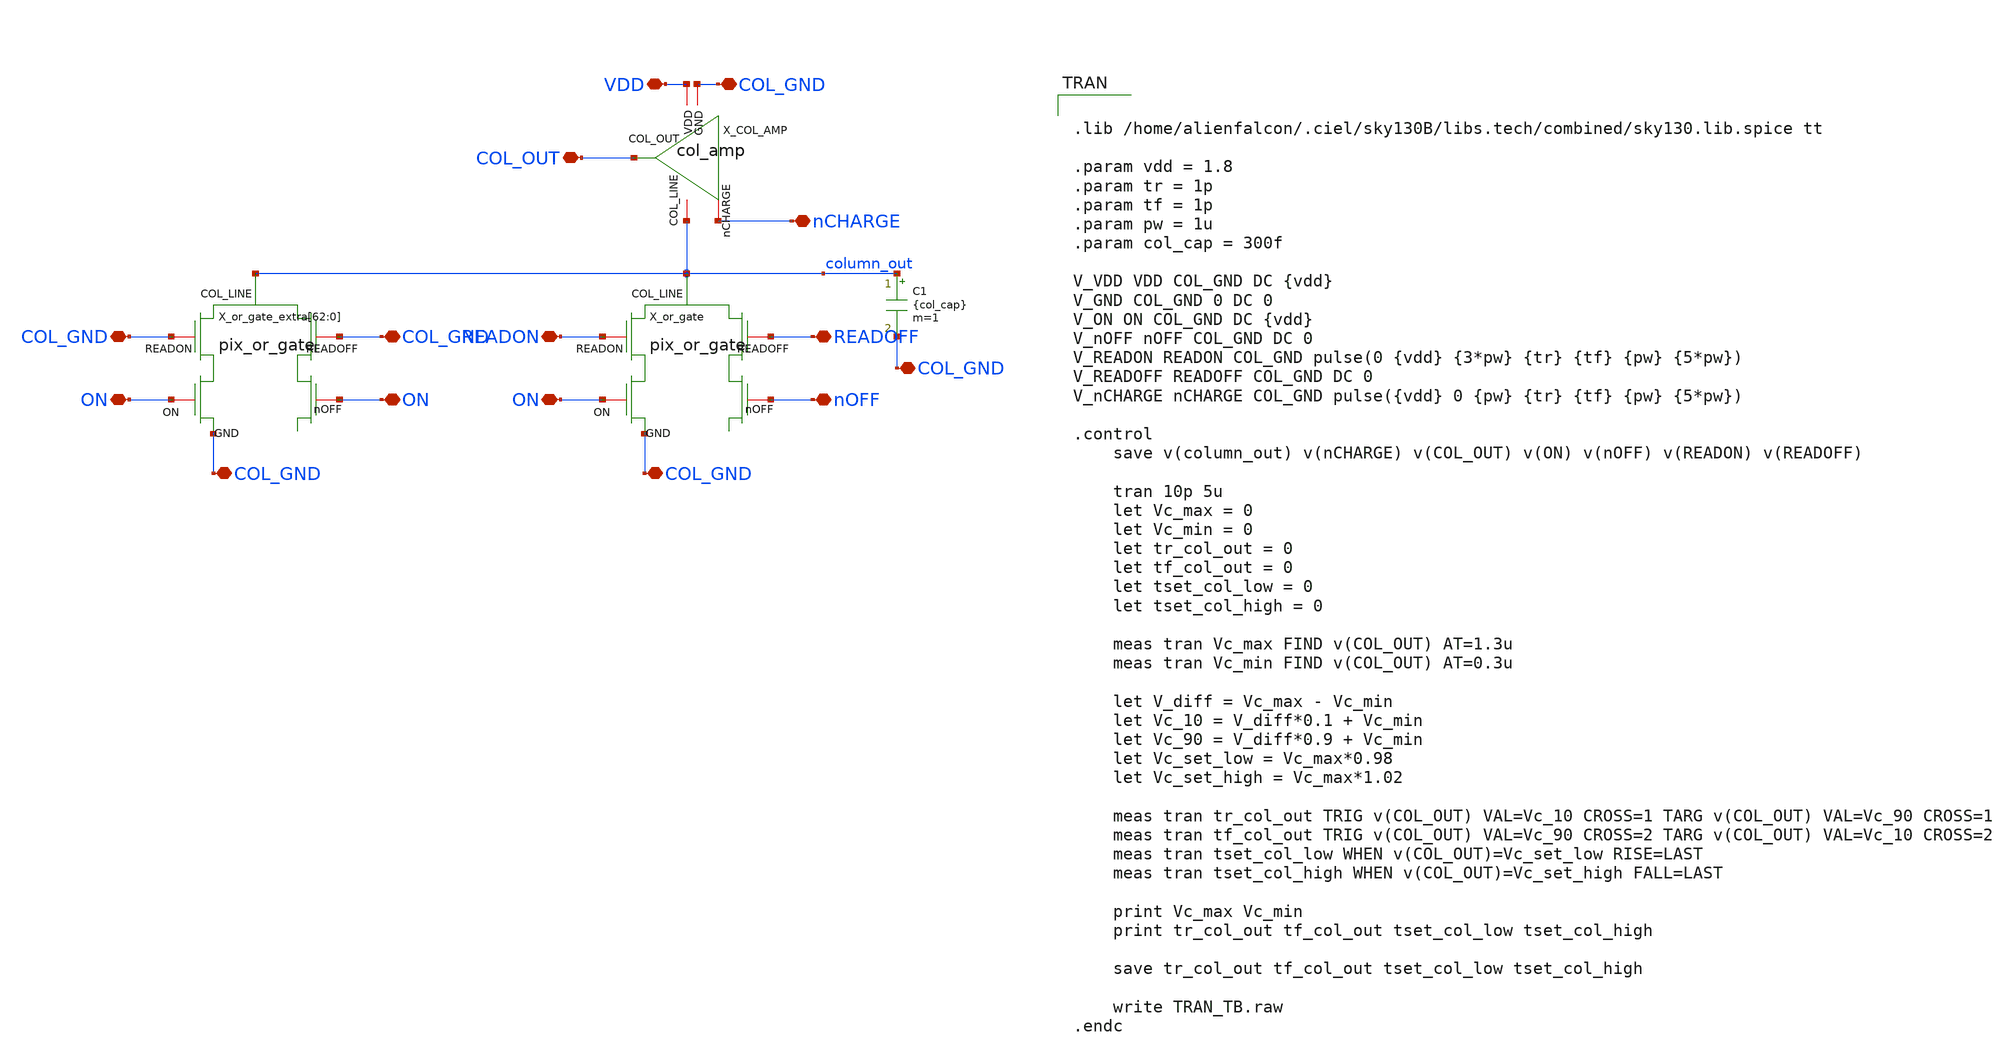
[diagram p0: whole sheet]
** sch_path: analog/xschem/col_amp_v2_std_vds/xschem/TRAN_TB.sch
**.subckt TRAN_TB nCHARGE nOFF READOFF ON READON COL_GND COL_GND COL_GND VDD COL_OUT COL_GND COL_GND
*+ COL_GND ON ON
*.iopin nCHARGE
*.iopin nOFF
*.iopin READOFF
*.iopin ON
*.iopin READON
*.iopin COL_GND
*.iopin COL_GND
*.iopin COL_GND
*.iopin VDD
*.iopin COL_OUT
*.iopin COL_GND
*.iopin COL_GND
*.iopin COL_GND
*.iopin ON
*.iopin ON
X_COL_AMP VDD nCHARGE COL_OUT COL_GND column_out col_amp
C1 column_out COL_GND {col_cap} m=1
X_or_gate column_out READOFF READON nOFF ON COL_GND pix_or_gate
X_or_gate_extra[62] column_out COL_GND COL_GND ON ON COL_GND pix_or_gate
X_or_gate_extra[61] column_out COL_GND COL_GND ON ON COL_GND pix_or_gate
X_or_gate_extra[60] column_out COL_GND COL_GND ON ON COL_GND pix_or_gate
X_or_gate_extra[59] column_out COL_GND COL_GND ON ON COL_GND pix_or_gate
X_or_gate_extra[58] column_out COL_GND COL_GND ON ON COL_GND pix_or_gate
X_or_gate_extra[57] column_out COL_GND COL_GND ON ON COL_GND pix_or_gate
X_or_gate_extra[56] column_out COL_GND COL_GND ON ON COL_GND pix_or_gate
X_or_gate_extra[55] column_out COL_GND COL_GND ON ON COL_GND pix_or_gate
X_or_gate_extra[54] column_out COL_GND COL_GND ON ON COL_GND pix_or_gate
X_or_gate_extra[53] column_out COL_GND COL_GND ON ON COL_GND pix_or_gate
X_or_gate_extra[52] column_out COL_GND COL_GND ON ON COL_GND pix_or_gate
X_or_gate_extra[51] column_out COL_GND COL_GND ON ON COL_GND pix_or_gate
X_or_gate_extra[50] column_out COL_GND COL_GND ON ON COL_GND pix_or_gate
X_or_gate_extra[49] column_out COL_GND COL_GND ON ON COL_GND pix_or_gate
X_or_gate_extra[48] column_out COL_GND COL_GND ON ON COL_GND pix_or_gate
X_or_gate_extra[47] column_out COL_GND COL_GND ON ON COL_GND pix_or_gate
X_or_gate_extra[46] column_out COL_GND COL_GND ON ON COL_GND pix_or_gate
X_or_gate_extra[45] column_out COL_GND COL_GND ON ON COL_GND pix_or_gate
X_or_gate_extra[44] column_out COL_GND COL_GND ON ON COL_GND pix_or_gate
X_or_gate_extra[43] column_out COL_GND COL_GND ON ON COL_GND pix_or_gate
X_or_gate_extra[42] column_out COL_GND COL_GND ON ON COL_GND pix_or_gate
X_or_gate_extra[41] column_out COL_GND COL_GND ON ON COL_GND pix_or_gate
X_or_gate_extra[40] column_out COL_GND COL_GND ON ON COL_GND pix_or_gate
X_or_gate_extra[39] column_out COL_GND COL_GND ON ON COL_GND pix_or_gate
X_or_gate_extra[38] column_out COL_GND COL_GND ON ON COL_GND pix_or_gate
X_or_gate_extra[37] column_out COL_GND COL_GND ON ON COL_GND pix_or_gate
X_or_gate_extra[36] column_out COL_GND COL_GND ON ON COL_GND pix_or_gate
X_or_gate_extra[35] column_out COL_GND COL_GND ON ON COL_GND pix_or_gate
X_or_gate_extra[34] column_out COL_GND COL_GND ON ON COL_GND pix_or_gate
X_or_gate_extra[33] column_out COL_GND COL_GND ON ON COL_GND pix_or_gate
X_or_gate_extra[32] column_out COL_GND COL_GND ON ON COL_GND pix_or_gate
X_or_gate_extra[31] column_out COL_GND COL_GND ON ON COL_GND pix_or_gate
X_or_gate_extra[30] column_out COL_GND COL_GND ON ON COL_GND pix_or_gate
X_or_gate_extra[29] column_out COL_GND COL_GND ON ON COL_GND pix_or_gate
X_or_gate_extra[28] column_out COL_GND COL_GND ON ON COL_GND pix_or_gate
X_or_gate_extra[27] column_out COL_GND COL_GND ON ON COL_GND pix_or_gate
X_or_gate_extra[26] column_out COL_GND COL_GND ON ON COL_GND pix_or_gate
X_or_gate_extra[25] column_out COL_GND COL_GND ON ON COL_GND pix_or_gate
X_or_gate_extra[24] column_out COL_GND COL_GND ON ON COL_GND pix_or_gate
X_or_gate_extra[23] column_out COL_GND COL_GND ON ON COL_GND pix_or_gate
X_or_gate_extra[22] column_out COL_GND COL_GND ON ON COL_GND pix_or_gate
X_or_gate_extra[21] column_out COL_GND COL_GND ON ON COL_GND pix_or_gate
X_or_gate_extra[20] column_out COL_GND COL_GND ON ON COL_GND pix_or_gate
X_or_gate_extra[19] column_out COL_GND COL_GND ON ON COL_GND pix_or_gate
X_or_gate_extra[18] column_out COL_GND COL_GND ON ON COL_GND pix_or_gate
X_or_gate_extra[17] column_out COL_GND COL_GND ON ON COL_GND pix_or_gate
X_or_gate_extra[16] column_out COL_GND COL_GND ON ON COL_GND pix_or_gate
X_or_gate_extra[15] column_out COL_GND COL_GND ON ON COL_GND pix_or_gate
X_or_gate_extra[14] column_out COL_GND COL_GND ON ON COL_GND pix_or_gate
X_or_gate_extra[13] column_out COL_GND COL_GND ON ON COL_GND pix_or_gate
X_or_gate_extra[12] column_out COL_GND COL_GND ON ON COL_GND pix_or_gate
X_or_gate_extra[11] column_out COL_GND COL_GND ON ON COL_GND pix_or_gate
X_or_gate_extra[10] column_out COL_GND COL_GND ON ON COL_GND pix_or_gate
X_or_gate_extra[9] column_out COL_GND COL_GND ON ON COL_GND pix_or_gate
X_or_gate_extra[8] column_out COL_GND COL_GND ON ON COL_GND pix_or_gate
X_or_gate_extra[7] column_out COL_GND COL_GND ON ON COL_GND pix_or_gate
X_or_gate_extra[6] column_out COL_GND COL_GND ON ON COL_GND pix_or_gate
X_or_gate_extra[5] column_out COL_GND COL_GND ON ON COL_GND pix_or_gate
X_or_gate_extra[4] column_out COL_GND COL_GND ON ON COL_GND pix_or_gate
X_or_gate_extra[3] column_out COL_GND COL_GND ON ON COL_GND pix_or_gate
X_or_gate_extra[2] column_out COL_GND COL_GND ON ON COL_GND pix_or_gate
X_or_gate_extra[1] column_out COL_GND COL_GND ON ON COL_GND pix_or_gate
X_or_gate_extra[0] column_out COL_GND COL_GND ON ON COL_GND pix_or_gate
**** begin user architecture code


.lib /home/alienfalcon/.ciel/sky130B/libs.tech/combined/sky130.lib.spice tt

.param vdd = 1.8
.param tr = 1p
.param tf = 1p
.param pw = 1u
.param col_cap = 300f

V_VDD VDD COL_GND DC {vdd}
V_GND COL_GND 0 DC 0
V_ON ON COL_GND DC {vdd}
V_nOFF nOFF COL_GND DC 0
V_READON READON COL_GND pulse(0 {vdd} {3*pw} {tr} {tf} {pw} {5*pw})
V_READOFF READOFF COL_GND DC 0
V_nCHARGE nCHARGE COL_GND pulse({vdd} 0 {pw} {tr} {tf} {pw} {5*pw})

.control
	save v(column_out) v(nCHARGE) v(COL_OUT) v(ON) v(nOFF) v(READON) v(READOFF)

	tran 10p 5u
	let Vc_max = 0
	let Vc_min = 0
	let tr_col_out = 0
	let tf_col_out = 0
	let tset_col_low = 0
	let tset_col_high = 0

	meas tran Vc_max FIND v(COL_OUT) AT=1.3u
	meas tran Vc_min FIND v(COL_OUT) AT=0.3u

	let V_diff = Vc_max - Vc_min
	let Vc_10 = V_diff*0.1 + Vc_min
	let Vc_90 = V_diff*0.9 + Vc_min
	let Vc_set_low = Vc_max*0.98
	let Vc_set_high = Vc_max*1.02

	meas tran tr_col_out TRIG v(COL_OUT) VAL=Vc_10 CROSS=1 TARG v(COL_OUT) VAL=Vc_90 CROSS=1
	meas tran tf_col_out TRIG v(COL_OUT) VAL=Vc_90 CROSS=2 TARG v(COL_OUT) VAL=Vc_10 CROSS=2
	meas tran tset_col_low WHEN v(COL_OUT)=Vc_set_low RISE=LAST
	meas tran tset_col_high WHEN v(COL_OUT)=Vc_set_high FALL=LAST

	print Vc_max Vc_min
	print tr_col_out tf_col_out tset_col_low tset_col_high

	save tr_col_out tf_col_out tset_col_low tset_col_high

	write TRAN_TB.raw
.endc




**** end user architecture code
**.ends
.end
